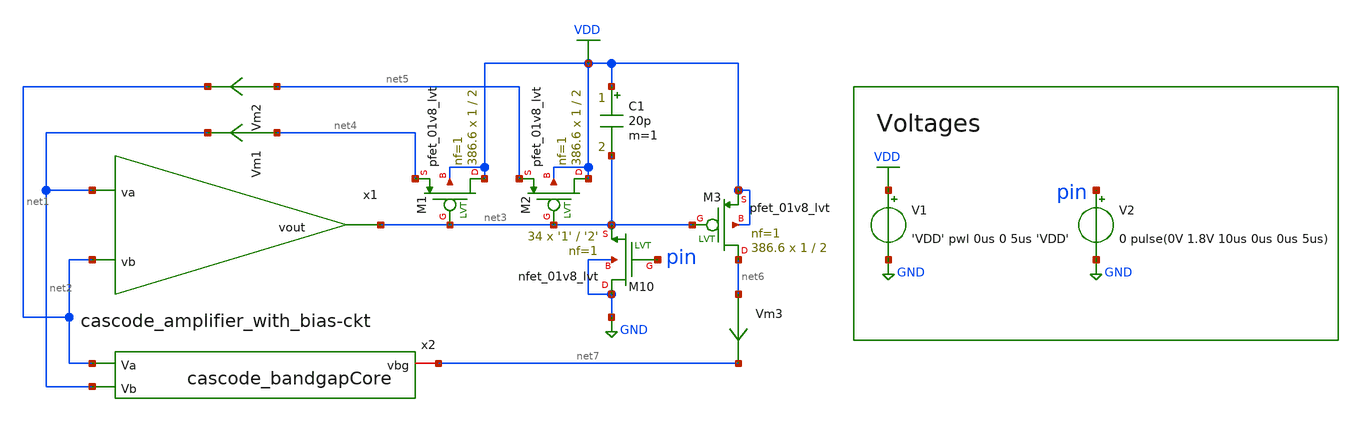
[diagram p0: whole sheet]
** sch_path: bandgap_sky130_v1/cascode_bandgap_real_op.sch
**.subckt cascode_bandgap_real_op
V1 VDD GND 'VDD' pwl 0us 0 5us 'VDD'
V2 pin GND 0 pulse(0V 1.8V 10us 0us 0us 5us)
C1 VDD net3 20p m=1
Vm1 net4 net2 0
.save i(vm1)
Vm2 net5 net1 0
.save i(vm2)
Vm3 net6 net7 0
.save i(vm3)
XM1 VDD net3 net4 VDD sky130_fd_pr__pfet_01v8_lvt L=2 W=1 nf=1 ad='int((nf+1)/2) * W/nf * 0.29' as='int((nf+2)/2) * W/nf * 0.29'
+ pd='2*int((nf+1)/2) * (W/nf + 0.29)' ps='2*int((nf+2)/2) * (W/nf + 0.29)' nrd='0.29 / W' nrs='0.29 / W'
+ sa=0 sb=0 sd=0 mult=386.6 m=386.6
XM2 VDD net3 net5 VDD sky130_fd_pr__pfet_01v8_lvt L=2 W=1 nf=1 ad='int((nf+1)/2) * W/nf * 0.29' as='int((nf+2)/2) * W/nf * 0.29'
+ pd='2*int((nf+1)/2) * (W/nf + 0.29)' ps='2*int((nf+2)/2) * (W/nf + 0.29)' nrd='0.29 / W' nrs='0.29 / W'
+ sa=0 sb=0 sd=0 mult=386.6 m=386.6
XM3 net6 net3 VDD VDD sky130_fd_pr__pfet_01v8_lvt L=2 W=1 nf=1 ad='int((nf+1)/2) * W/nf * 0.29' as='int((nf+2)/2) * W/nf * 0.29'
+ pd='2*int((nf+1)/2) * (W/nf + 0.29)' ps='2*int((nf+2)/2) * (W/nf + 0.29)' nrd='0.29 / W' nrs='0.29 / W'
+ sa=0 sb=0 sd=0 mult=386.6 m=386.6
XM10 GND pin net3 GND sky130_fd_pr__nfet_01v8_lvt L='2' W='1' nf=1 ad='int((nf+1)/2) * W/nf * 0.29' as='int((nf+2)/2) * W/nf * 0.29'
+ pd='2*int((nf+1)/2) * (W/nf + 0.29)' ps='2*int((nf+2)/2) * (W/nf + 0.29)' nrd='0.29 / W' nrs='0.29 / W'
+ sa=0 sb=0 sd=0 mult=34 m=34
x1 net2 net1 net3 cascode_amplifier_with_bias-ckt
x2 net1 net2 net7 cascode_bandgapCore
**** begin user architecture code

** opencircuitdesign pdks install
.lib $::SKYWATER_MODELS/sky130.lib.spice tt


**** end user architecture code
**.ends

* expanding   symbol:
*+  /home/thomas/Projects/bandgapReferenceCircuit/bandgap_sky130_v1/cascode_amplifier_with_bias-ckt.sym # of pins=3
** sym_path: bandgap_sky130_v1/cascode_amplifier_with_bias-ckt.sym
** sch_path: bandgap_sky130_v1/cascode_amplifier_with_bias-ckt.sch
.subckt cascode_amplifier_with_bias-ckt va vb vout
*.ipin va
*.ipin vb
*.opin vout
XM5 vout vb Vq GND sky130_fd_pr__nfet_01v8_lvt L='2' W='1' nf=1 ad='int((nf+1)/2) * W/nf * 0.29' as='int((nf+2)/2) * W/nf * 0.29'
+ pd='2*int((nf+1)/2) * (W/nf + 0.29)' ps='2*int((nf+2)/2) * (W/nf + 0.29)' nrd='0.29 / W' nrs='0.29 / W'
+ sa=0 sb=0 sd=0 mult=26.95 m=26.95
XM6 Vq Vx GND GND sky130_fd_pr__nfet_01v8_lvt L=2 W=1 nf=1 ad='int((nf+1)/2) * W/nf * 0.29' as='int((nf+2)/2) * W/nf * 0.29'
+ pd='2*int((nf+1)/2) * (W/nf + 0.29)' ps='2*int((nf+2)/2) * (W/nf + 0.29)' nrd='0.29 / W' nrs='0.29 / W'
+ sa=0 sb=0 sd=0 mult=3.65 m=3.65
XM9 vg va Vq GND sky130_fd_pr__nfet_01v8_lvt L='2' W='1' nf=1 ad='int((nf+1)/2) * W/nf * 0.29' as='int((nf+2)/2) * W/nf * 0.29'
+ pd='2*int((nf+1)/2) * (W/nf + 0.29)' ps='2*int((nf+2)/2) * (W/nf + 0.29)' nrd='0.29 / W' nrs='0.29 / W'
+ sa=0 sb=0 sd=0 mult=26.95 m=26.95
XM7 Vx Vx GND GND sky130_fd_pr__nfet_01v8_lvt L=2 W=1 nf=1 ad='int((nf+1)/2) * W/nf * 0.29' as='int((nf+2)/2) * W/nf * 0.29'
+ pd='2*int((nf+1)/2) * (W/nf + 0.29)' ps='2*int((nf+2)/2) * (W/nf + 0.29)' nrd='0.29 / W' nrs='0.29 / W'
+ sa=0 sb=0 sd=0 mult=3.65 m=3.65
XM13 Vx vout VDD VDD sky130_fd_pr__pfet_01v8_lvt L=2 W=1 nf=1 ad='int((nf+1)/2) * W/nf * 0.29' as='int((nf+2)/2) * W/nf * 0.29'
+ pd='2*int((nf+1)/2) * (W/nf + 0.29)' ps='2*int((nf+2)/2) * (W/nf + 0.29)' nrd='0.29 / W' nrs='0.29 / W'
+ sa=0 sb=0 sd=0 mult=77.32 m=77.32
XM4 vg vg VDD VDD sky130_fd_pr__pfet_01v8_lvt L=2 W=1 nf=1 ad='int((nf+1)/2) * W/nf * 0.29' as='int((nf+2)/2) * W/nf * 0.29'
+ pd='2*int((nf+1)/2) * (W/nf + 0.29)' ps='2*int((nf+2)/2) * (W/nf + 0.29)' nrd='0.29 / W' nrs='0.29 / W'
+ sa=0 sb=0 sd=0 mult=38.66 m=38.66
XM8 vout vg VDD VDD sky130_fd_pr__pfet_01v8_lvt L=2 W=1 nf=1 ad='int((nf+1)/2) * W/nf * 0.29' as='int((nf+2)/2) * W/nf * 0.29'
+ pd='2*int((nf+1)/2) * (W/nf + 0.29)' ps='2*int((nf+2)/2) * (W/nf + 0.29)' nrd='0.29 / W' nrs='0.29 / W'
+ sa=0 sb=0 sd=0 mult=38.66 m=38.66
.ends


* expanding   symbol:
*+  /home/thomas/Projects/bandgapReferenceCircuit/bandgap_sky130_v1/cascode_bandgapCore.sym # of pins=3
** sym_path: bandgap_sky130_v1/cascode_bandgapCore.sym
** sch_path: bandgap_sky130_v1/cascode_bandgapCore.sch
.subckt cascode_bandgapCore Va Vb vbg
*.ipin Va
*.ipin Vb
*.iopin vbg
XQ2 GND GND Veb sky130_fd_pr__pnp_05v5_W3p40L3p40 m=1
Vr4 net1 net3 0
.save i(vr4)
Vr2 net1 net2 0
.save i(vr2)
Vr1 Va net4 0
.save i(vr1)
Vq2 Va Veb 0
.save i(vq2)
XQ1 GND GND vbneg sky130_fd_pr__pnp_05v5_W3p40L3p40 m=39
XR1 GND net4 GND sky130_fd_pr__res_xhigh_po_0p35 L=21.839 mult=1 m=1
XR2 GND net3 GND sky130_fd_pr__res_xhigh_po_0p35 L=21.839 mult=1 m=1
XR3 vbneg net2 GND sky130_fd_pr__res_xhigh_po_0p35 L=3.763 mult=1 m=1
XR6 GND vbg GND sky130_fd_pr__res_xhigh_po_0p35 L=17.38 mult=1 m=1
x1 Va net1 vgate cascode_amplifier_with_bias-ckt
C2 Va GND 20p m=1
Vm1 net6 Va 0
.save i(vm1)
Vm2 net5 net1 0
.save i(vm2)
XM1 net6 vgate VDD VDD sky130_fd_pr__pfet_01v8_lvt L=2 W=1 nf=1 ad='int((nf+1)/2) * W/nf * 0.29' as='int((nf+2)/2) * W/nf * 0.29'
+ pd='2*int((nf+1)/2) * (W/nf + 0.29)' ps='2*int((nf+2)/2) * (W/nf + 0.29)' nrd='0.29 / W' nrs='0.29 / W'
+ sa=0 sb=0 sd=0 mult=386.6 m=386.6
XM2 net5 vgate VDD VDD sky130_fd_pr__pfet_01v8_lvt L=2 W=1 nf=1 ad='int((nf+1)/2) * W/nf * 0.29' as='int((nf+2)/2) * W/nf * 0.29'
+ pd='2*int((nf+1)/2) * (W/nf + 0.29)' ps='2*int((nf+2)/2) * (W/nf + 0.29)' nrd='0.29 / W' nrs='0.29 / W'
+ sa=0 sb=0 sd=0 mult=386.6 m=386.6
XM10 vgate porst GND GND sky130_fd_pr__nfet_01v8_lvt L='2' W='1' nf=1 ad='int((nf+1)/2) * W/nf * 0.29'
+ as='int((nf+2)/2) * W/nf * 0.29' pd='2*int((nf+1)/2) * (W/nf + 0.29)' ps='2*int((nf+2)/2) * (W/nf + 0.29)'
+ nrd='0.29 / W' nrs='0.29 / W' sa=0 sb=0 sd=0 mult=34 m=34
Vm3 net7 vbg 0
.save i(vm3)
XM3 net7 vgate VDD VDD sky130_fd_pr__pfet_01v8_lvt L=2 W=1 nf=1 ad='int((nf+1)/2) * W/nf * 0.29' as='int((nf+2)/2) * W/nf * 0.29'
+ pd='2*int((nf+1)/2) * (W/nf + 0.29)' ps='2*int((nf+2)/2) * (W/nf + 0.29)' nrd='0.29 / W' nrs='0.29 / W'
+ sa=0 sb=0 sd=0 mult=386.6 m=386.6
.ends

.GLOBAL VDD
.GLOBAL GND
.end
